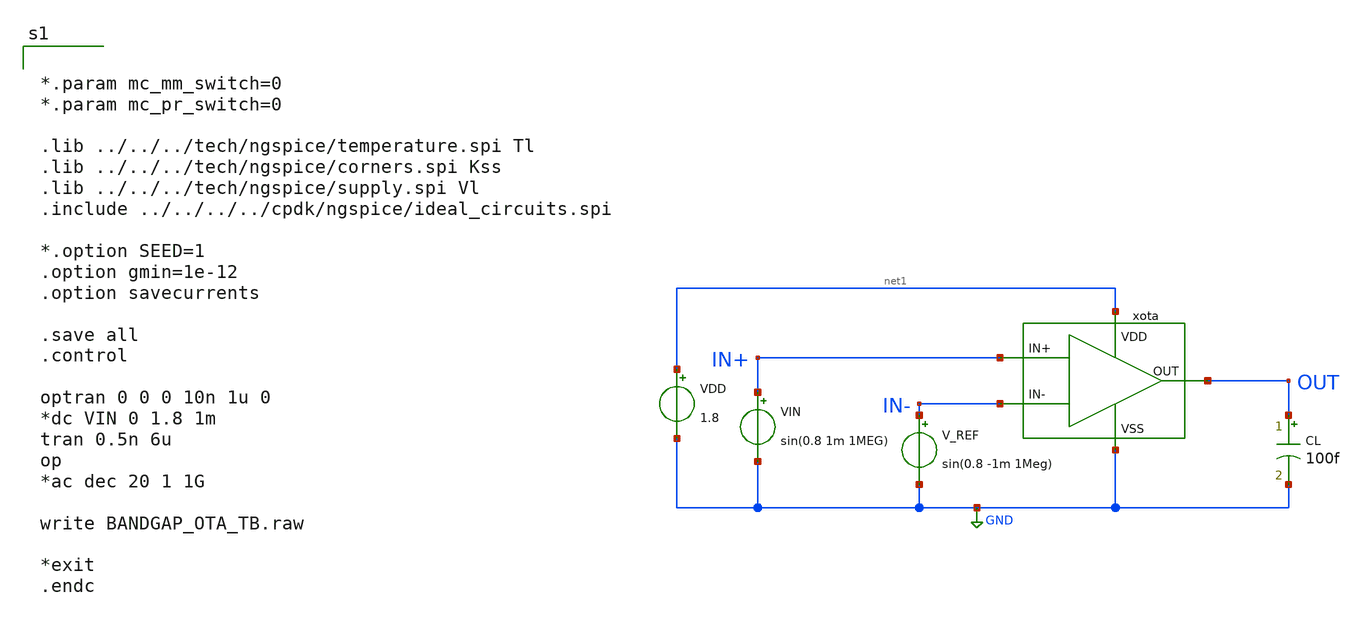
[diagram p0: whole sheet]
** sch_path: design/LELO_GR03_SKY130A/BANDGAP_OTA_TB.sch
**.subckt BANDGAP_OTA_TB
xota net1 IN- IN+ OUT GND BANDGAP_OTA
CL OUT GND 100f m=1
VIN IN+ GND sin(0.8 1m 1MEG)
V_REF IN- GND sin(0.8 -1m 1Meg)
VDD net1 GND 1.8
**** begin user architecture code


*.param mc_mm_switch=0
*.param mc_pr_switch=0

.lib ../../../tech/ngspice/temperature.spi Tl
.lib ../../../tech/ngspice/corners.spi Kss
.lib ../../../tech/ngspice/supply.spi Vl
.include ../../../../cpdk/ngspice/ideal_circuits.spi

*.option SEED=1
.option gmin=1e-12
.option savecurrents

.save all
.control

optran 0 0 0 10n 1u 0
*dc VIN 0 1.8 1m
tran 0.5n 6u
op
*ac dec 20 1 1G

write BANDGAP_OTA_TB.raw

*exit
.endc



**** end user architecture code
**.ends
.GLOBAL GND
.end
